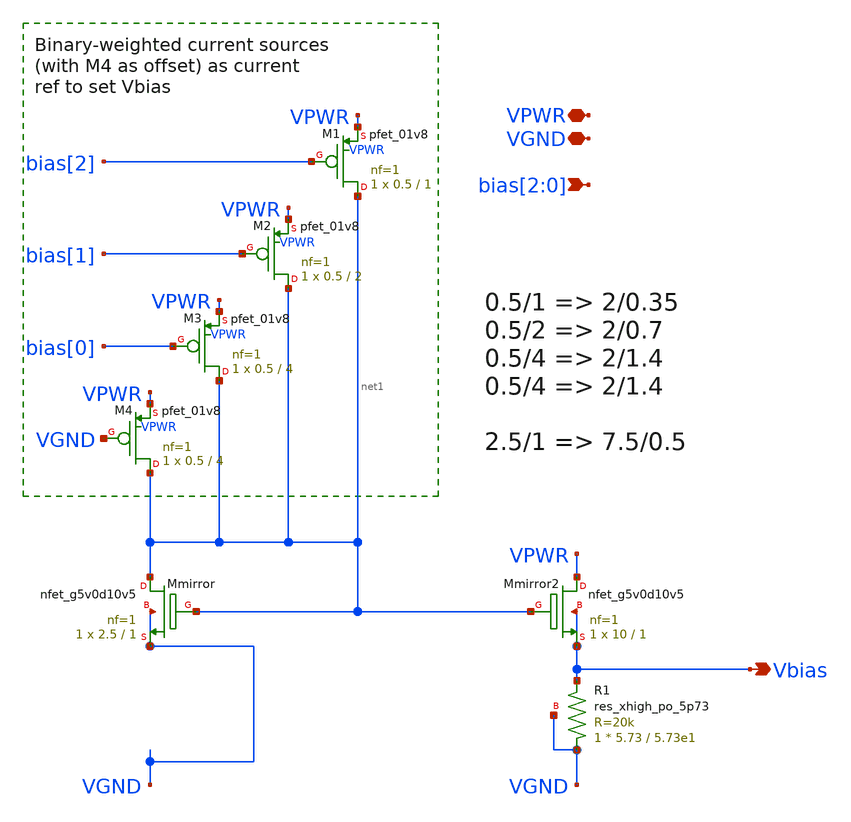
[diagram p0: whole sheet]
** sch_path: xschem-cascode-backup/vbiasSF.sch
**.subckt vbiasSF VPWR VGND bias[2],bias[1],bias[0] Vbias
*.iopin VPWR
*.iopin VGND
*.ipin bias[2],bias[1],bias[0]
*.opin Vbias
XM1 net1 bias[2] VPWR VPWR sky130_fd_pr__pfet_01v8 L=1 W=0.5 nf=1 ad='int((nf+1)/2) * W/nf * 0.29' as='int((nf+2)/2) * W/nf * 0.29'
+ pd='2*int((nf+1)/2) * (W/nf + 0.29)' ps='2*int((nf+2)/2) * (W/nf + 0.29)' nrd='0.29 / W' nrs='0.29 / W'
+ sa=0 sb=0 sd=0 mult=1 m=1
XM2 net1 bias[1] VPWR VPWR sky130_fd_pr__pfet_01v8 L=2 W=0.5 nf=1 ad='int((nf+1)/2) * W/nf * 0.29' as='int((nf+2)/2) * W/nf * 0.29'
+ pd='2*int((nf+1)/2) * (W/nf + 0.29)' ps='2*int((nf+2)/2) * (W/nf + 0.29)' nrd='0.29 / W' nrs='0.29 / W'
+ sa=0 sb=0 sd=0 mult=1 m=1
XM3 net1 bias[0] VPWR VPWR sky130_fd_pr__pfet_01v8 L=4 W=0.5 nf=1 ad='int((nf+1)/2) * W/nf * 0.29' as='int((nf+2)/2) * W/nf * 0.29'
+ pd='2*int((nf+1)/2) * (W/nf + 0.29)' ps='2*int((nf+2)/2) * (W/nf + 0.29)' nrd='0.29 / W' nrs='0.29 / W'
+ sa=0 sb=0 sd=0 mult=1 m=1
XMmirror net1 net1 VGND VGND sky130_fd_pr__nfet_g5v0d10v5 L=1 W=2.5 nf=1 ad='int((nf+1)/2) * W/nf * 0.29'
+ as='int((nf+2)/2) * W/nf * 0.29' pd='2*int((nf+1)/2) * (W/nf + 0.29)' ps='2*int((nf+2)/2) * (W/nf + 0.29)'
+ nrd='0.29 / W' nrs='0.29 / W' sa=0 sb=0 sd=0 mult=1 m=1
XM4 net1 VGND VPWR VPWR sky130_fd_pr__pfet_01v8 L=4 W=0.5 nf=1 ad='int((nf+1)/2) * W/nf * 0.29' as='int((nf+2)/2) * W/nf * 0.29'
+ pd='2*int((nf+1)/2) * (W/nf + 0.29)' ps='2*int((nf+2)/2) * (W/nf + 0.29)' nrd='0.29 / W' nrs='0.29 / W'
+ sa=0 sb=0 sd=0 mult=1 m=1
XMmirror2 VPWR net1 Vbias Vbias sky130_fd_pr__nfet_g5v0d10v5 L=1 W=10 nf=1 ad='int((nf+1)/2) * W/nf * 0.29'
+ as='int((nf+2)/2) * W/nf * 0.29' pd='2*int((nf+1)/2) * (W/nf + 0.29)' ps='2*int((nf+2)/2) * (W/nf + 0.29)'
+ nrd='0.29 / W' nrs='0.29 / W' sa=0 sb=0 sd=0 mult=1 m=1
XR1 VGND Vbias VGND sky130_fd_pr__res_xhigh_po_5p73 L=5.73e1 mult=1 m=1
**.ends
.end
